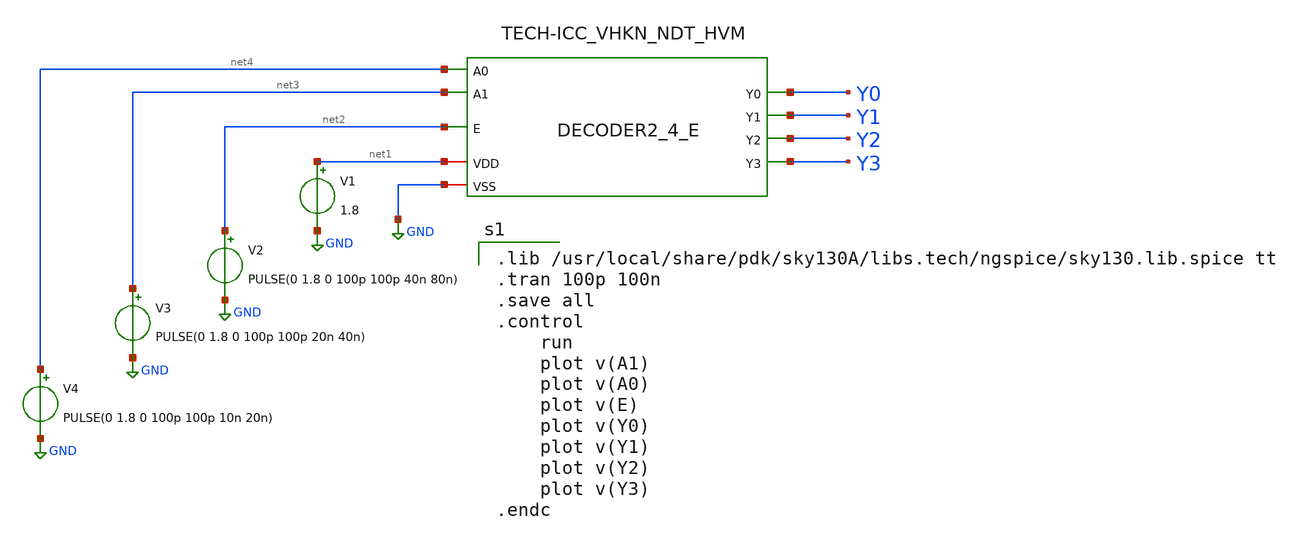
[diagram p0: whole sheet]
** sch_path: DECODER3TO8/Schematic/CMOS_DECODER2_4_E.sch
**.subckt CMOS_DECODER2_4_E
x1 net1 net4 Y0 net3 Y1 Y2 Y3 GND net2 DECODER2_4_E
V1 net1 GND 1.8
V2 net2 GND PULSE(0 1.8 0 100p 100p 40n 80n)
V3 net3 GND PULSE(0 1.8 0 100p 100p 20n 40n)
V4 net4 GND PULSE(0 1.8 0 100p 100p 10n 20n)
**** begin user architecture code

.lib /usr/local/share/pdk/sky130A/libs.tech/ngspice/sky130.lib.spice tt
.tran 100p 100n
.save all
.control
    run
    plot v(A1)
    plot v(A0)
    plot v(E)
    plot v(Y0)
    plot v(Y1)
    plot v(Y2)
    plot v(Y3)
.endc


**** end user architecture code
**.ends
.GLOBAL GND
.end
